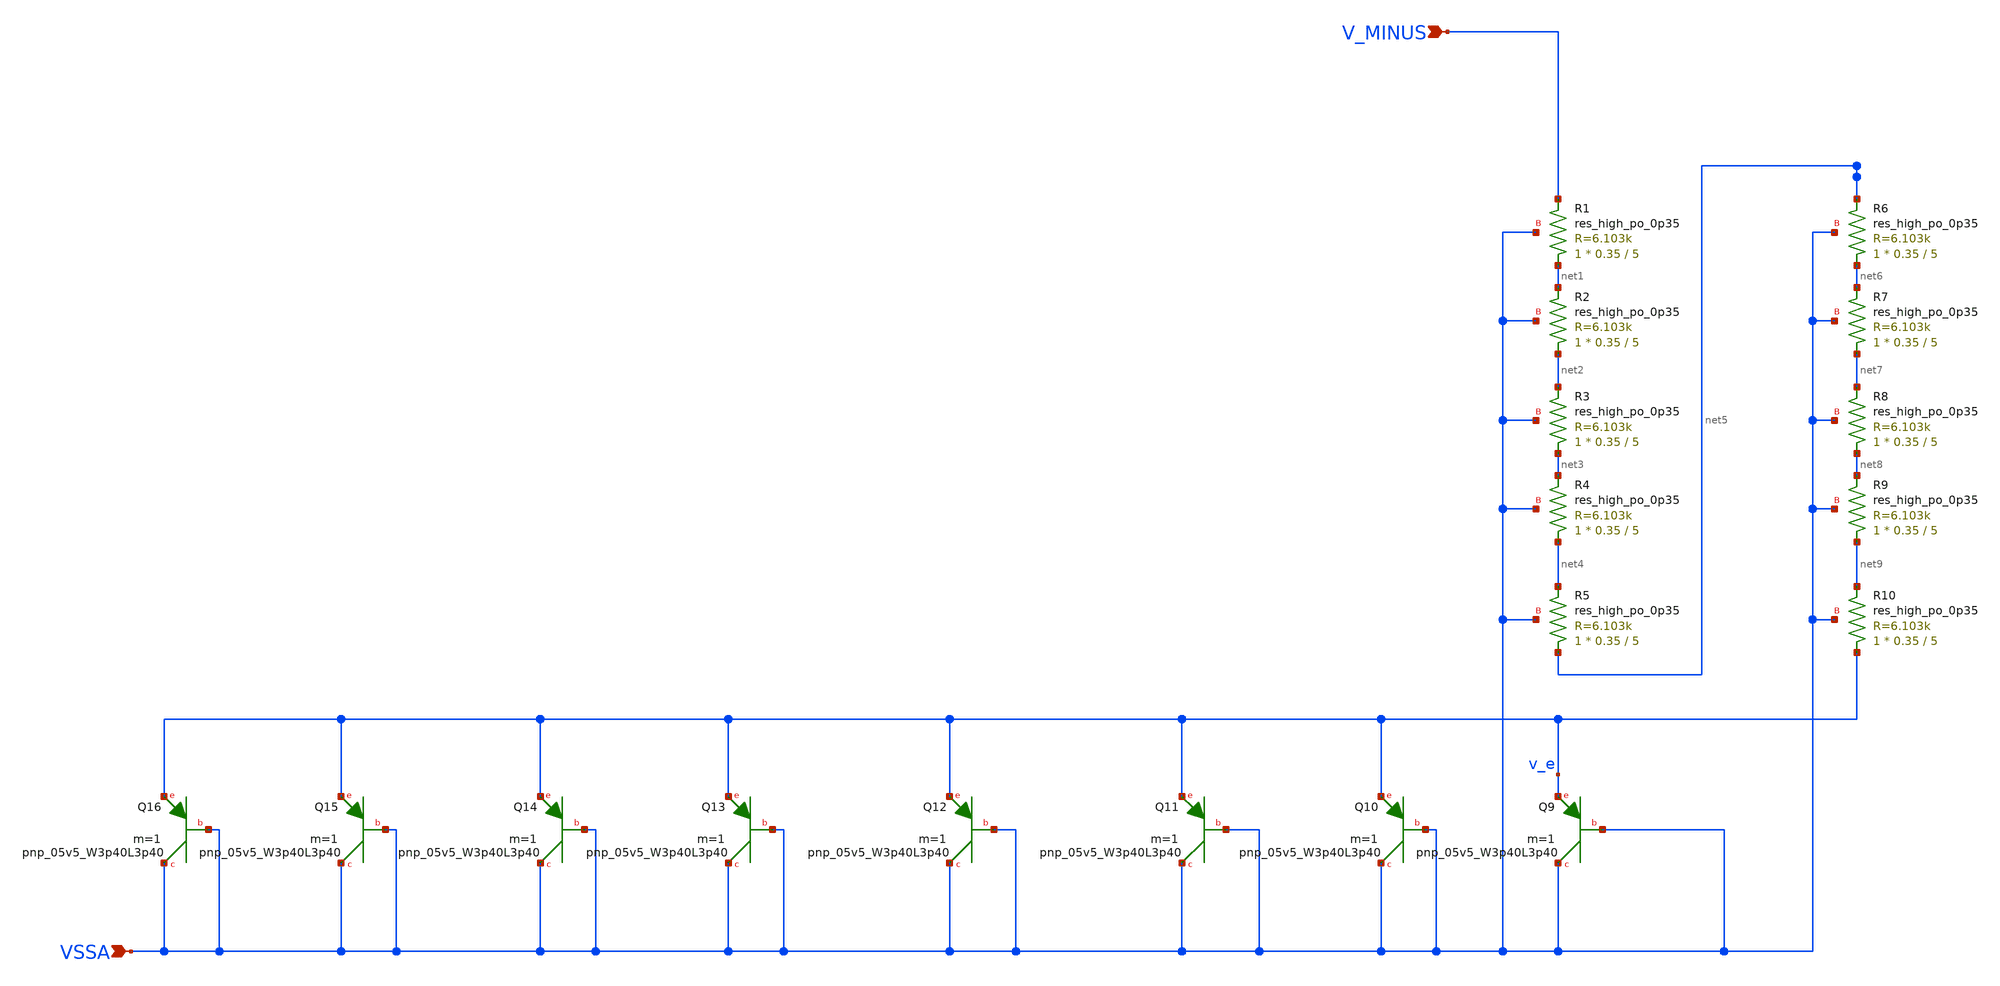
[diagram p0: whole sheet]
** sch_path: gds/bg2_vminus_branch.sch
**.subckt bg2_vminus_branch VSSA V_MINUS
*.ipin VSSA
*.ipin V_MINUS
XQ9 VSSA VSSA v_e sky130_fd_pr__pnp_05v5_W3p40L3p40 m=1
XR1 net1 V_MINUS VSSA sky130_fd_pr__res_high_po_0p35 L=5 mult=1 m=1
XR2 net2 net1 VSSA sky130_fd_pr__res_high_po_0p35 L=5 mult=1 m=1
XQ10 VSSA VSSA v_e sky130_fd_pr__pnp_05v5_W3p40L3p40 m=1
XQ11 VSSA VSSA v_e sky130_fd_pr__pnp_05v5_W3p40L3p40 m=1
XQ12 VSSA VSSA v_e sky130_fd_pr__pnp_05v5_W3p40L3p40 m=1
XQ13 VSSA VSSA v_e sky130_fd_pr__pnp_05v5_W3p40L3p40 m=1
XQ14 VSSA VSSA v_e sky130_fd_pr__pnp_05v5_W3p40L3p40 m=1
XQ15 VSSA VSSA v_e sky130_fd_pr__pnp_05v5_W3p40L3p40 m=1
XQ16 VSSA VSSA v_e sky130_fd_pr__pnp_05v5_W3p40L3p40 m=1
XR3 net3 net2 VSSA sky130_fd_pr__res_high_po_0p35 L=5 mult=1 m=1
XR4 net4 net3 VSSA sky130_fd_pr__res_high_po_0p35 L=5 mult=1 m=1
XR5 net5 net4 VSSA sky130_fd_pr__res_high_po_0p35 L=5 mult=1 m=1
XR6 net6 net5 VSSA sky130_fd_pr__res_high_po_0p35 L=5 mult=1 m=1
XR7 net7 net6 VSSA sky130_fd_pr__res_high_po_0p35 L=5 mult=1 m=1
XR8 net8 net7 VSSA sky130_fd_pr__res_high_po_0p35 L=5 mult=1 m=1
XR9 net9 net8 VSSA sky130_fd_pr__res_high_po_0p35 L=5 mult=1 m=1
XR10 v_e net9 VSSA sky130_fd_pr__res_high_po_0p35 L=5 mult=1 m=1
**.ends
.end
